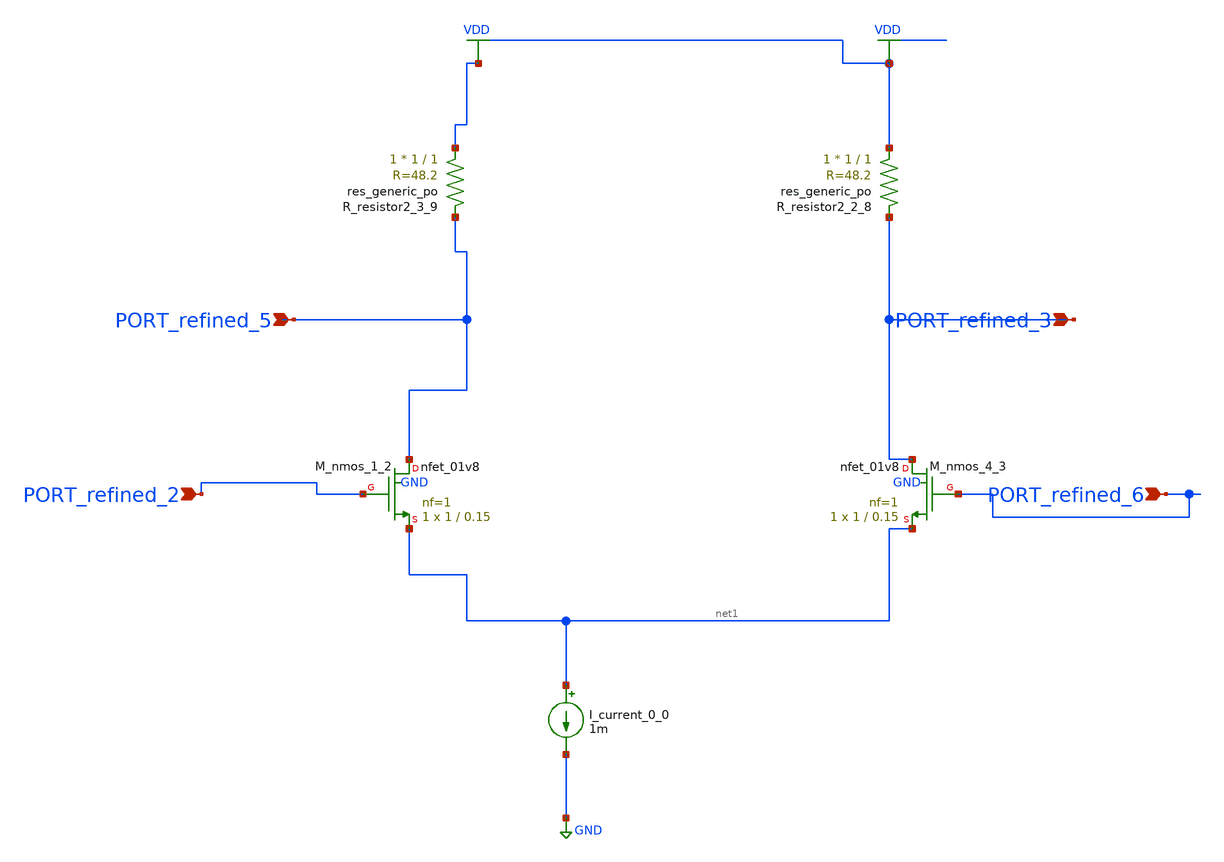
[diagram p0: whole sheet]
** sch_path: schematics/AMSNet/201.sch
**.subckt 201 PORT_refined_6 PORT_refined_5 PORT_refined_2 PORT_refined_3
*.ipin PORT_refined_6
*.ipin PORT_refined_5
*.ipin PORT_refined_2
*.ipin PORT_refined_3
I_current_0_0 net1 GND 1m
XM_nmos_1_2 PORT_refined_5 PORT_refined_2 net1 GND sky130_fd_pr__nfet_01v8 L=0.15 W=1 nf=1 ad='int((1 + 1)/2) * 1 / 1 * 0.29'
+ as='int((1 + 2)/2) * 1 / 1 * 0.29' pd='2*int((1 + 1)/2) * (1 / 1 + 0.29)' ps='2*int((1 + 2)/2) * (1 / 1 + 0.29)'
+ nrd='0.29 / 1 ' nrs='0.29 / 1 ' sa=0 sb=0 sd=0 mult=1 m=1
XM_nmos_4_3 PORT_refined_3 PORT_refined_6 net1 GND sky130_fd_pr__nfet_01v8 L=0.15 W=1 nf=1 ad='int((1 + 1)/2) * 1 / 1 * 0.29'
+ as='int((1 + 2)/2) * 1 / 1 * 0.29' pd='2*int((1 + 1)/2) * (1 / 1 + 0.29)' ps='2*int((1 + 2)/2) * (1 / 1 + 0.29)'
+ nrd='0.29 / 1 ' nrs='0.29 / 1 ' sa=0 sb=0 sd=0 mult=1 m=1
XR_resistor2_2_8 VDD PORT_refined_3 sky130_fd_pr__res_generic_po W=1 L=1 m=1
XR_resistor2_3_9 VDD PORT_refined_5 sky130_fd_pr__res_generic_po W=1 L=1 m=1
**.ends
.GLOBAL GND
.GLOBAL VDD
.end
